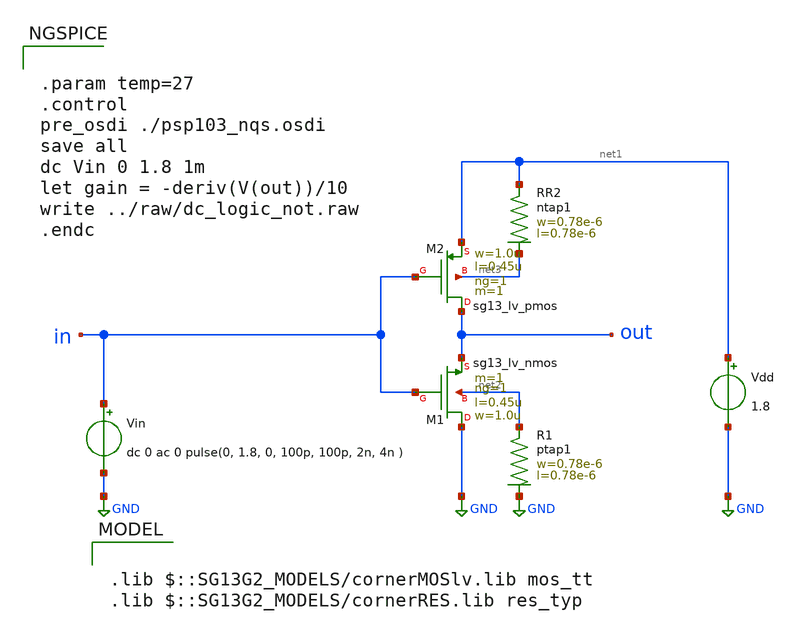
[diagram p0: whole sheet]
** sch_path: ihp-sg13g2/libs.tech/xschem/sg13g2_tests/dc_logic_not.sch
* Copyright 2023 IHP PDK Authors
**.subckt dc_logic_not
Vin in GND dc 0 ac 0 pulse(0, 1.8, 0, 100p, 100p, 2n, 4n )
Vdd net1 GND 1.8
XM1 GND in out net2 sg13_lv_nmos w=1.0u l=0.45u ng=1 m=1 mm_ok=1
XR1 net2 GND ptap1 R=262.8 w=0.78e-6 l=0.78e-6
XR2 net1 net3 ntap1 R=262.8 w=0.78e-6 l=0.78e-6
XM2 out in net1 net3 sg13_lv_pmos w=1.0u l=0.45u ng=1 m=1 mm_ok=1
**** begin user architecture code

.lib $::SG13G2_MODELS/cornerMOSlv.lib mos_tt
.lib $::SG13G2_MODELS/cornerRES.lib res_typ



.param temp=27
.control
pre_osdi ./psp103_nqs.osdi
save all
dc Vin 0 1.8 1m
let gain = -deriv(V(out))/10
write ../raw/dc_logic_not.raw
.endc


**** end user architecture code
**.ends
.GLOBAL GND
.end
